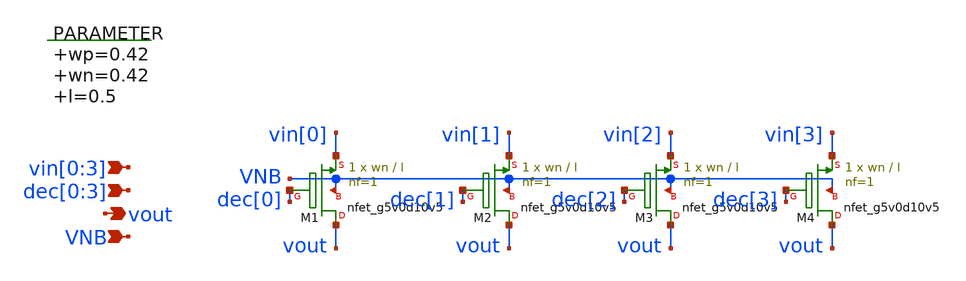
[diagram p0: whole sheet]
** sch_path: xschem/vselector_6b_1v_stage_3.sch
**.subckt vselector_6b_1v_stage_3 vin[0],vin[1],vin[2],vin[3] vout VNB dec[0],dec[1],dec[2],dec[3]
*.ipin vin[0],vin[1],vin[2],vin[3]
*.opin vout
*.ipin VNB
*.ipin dec[0],dec[1],dec[2],dec[3]
.param wp=0.42 wn=0.42 l=0.5

XM1 vout dec[0] vin[0] VNB sky130_fd_pr__nfet_g5v0d10v5 L=l W=wn nf=1 ad='int((nf+1)/2) * W/nf * 0.29'
+ as='int((nf+2)/2) * W/nf * 0.29' pd='2*int((nf+1)/2) * (W/nf + 0.29)' ps='2*int((nf+2)/2) * (W/nf + 0.29)'
+ nrd='0.29 / W' nrs='0.29 / W' sa=0 sb=0 sd=0 mult=1 m=1
XM2 vout dec[1] vin[1] VNB sky130_fd_pr__nfet_g5v0d10v5 L=l W=wn nf=1 ad='int((nf+1)/2) * W/nf * 0.29'
+ as='int((nf+2)/2) * W/nf * 0.29' pd='2*int((nf+1)/2) * (W/nf + 0.29)' ps='2*int((nf+2)/2) * (W/nf + 0.29)'
+ nrd='0.29 / W' nrs='0.29 / W' sa=0 sb=0 sd=0 mult=1 m=1
XM3 vout dec[2] vin[2] VNB sky130_fd_pr__nfet_g5v0d10v5 L=l W=wn nf=1 ad='int((nf+1)/2) * W/nf * 0.29'
+ as='int((nf+2)/2) * W/nf * 0.29' pd='2*int((nf+1)/2) * (W/nf + 0.29)' ps='2*int((nf+2)/2) * (W/nf + 0.29)'
+ nrd='0.29 / W' nrs='0.29 / W' sa=0 sb=0 sd=0 mult=1 m=1
XM4 vout dec[3] vin[3] VNB sky130_fd_pr__nfet_g5v0d10v5 L=l W=wn nf=1 ad='int((nf+1)/2) * W/nf * 0.29'
+ as='int((nf+2)/2) * W/nf * 0.29' pd='2*int((nf+1)/2) * (W/nf + 0.29)' ps='2*int((nf+2)/2) * (W/nf + 0.29)'
+ nrd='0.29 / W' nrs='0.29 / W' sa=0 sb=0 sd=0 mult=1 m=1
**.ends
.end
